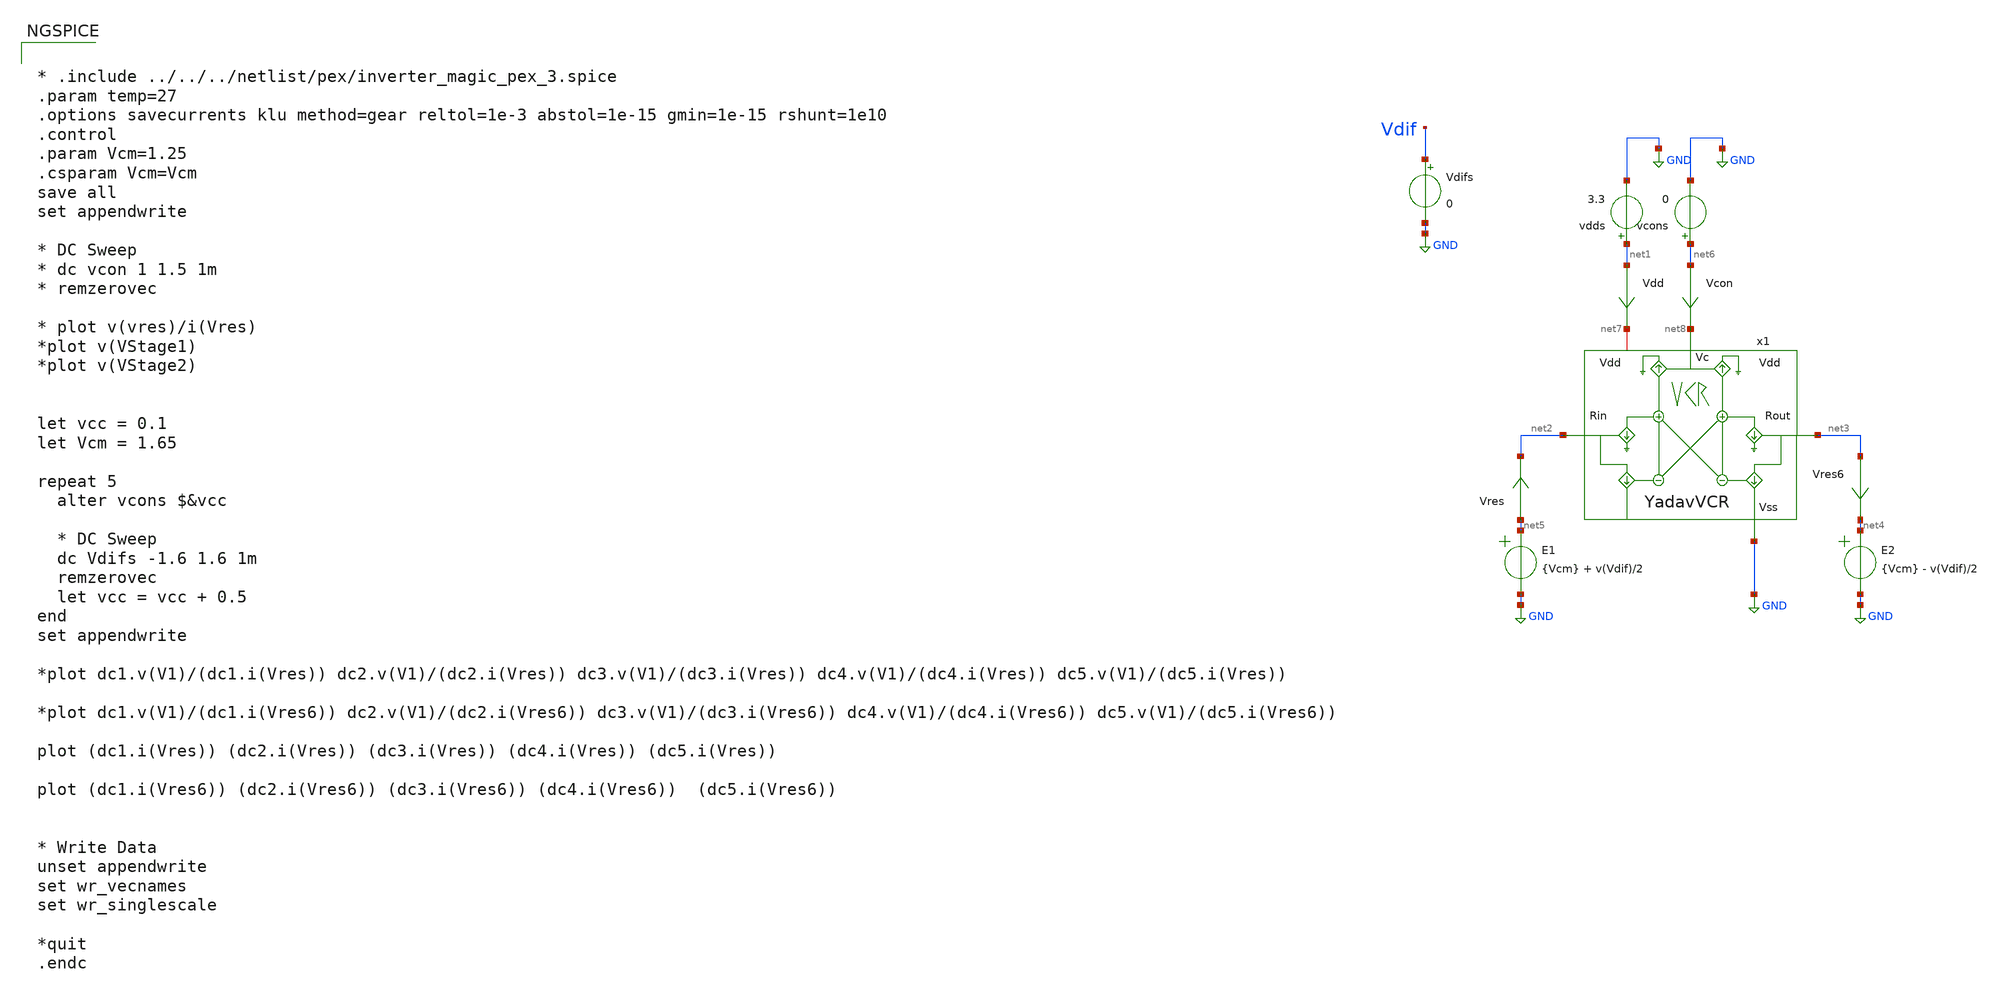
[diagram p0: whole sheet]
** sch_path: macros/heichips26_analog_project/macros/yadav/testbenches/xschem/plm.sch
**.subckt plm
Vres net5 net2 0
.save i(vres)
vdds net1 GND 3.3
Vdd net1 net7 0
.save i(vdd)
Vres6 net3 net4 0
.save i(vres6)
E1 net5 GND VOL=' {Vcm} + v(Vdif)/2 '
E2 net4 GND VOL=' {Vcm} - v(Vdif)/2 '
Vdifs Vdif GND 0
x1 net7 net2 net3 net8 GND YadavVCR
vcons net6 GND 0
Vcon net6 net8 0
.save i(vcon)
**** begin user architecture code


* .include ../../../netlist/pex/inverter_magic_pex_3.spice
.param temp=27
.options savecurrents klu method=gear reltol=1e-3 abstol=1e-15 gmin=1e-15 rshunt=1e10
.control
.param Vcm=1.25
.csparam Vcm=Vcm
save all
set appendwrite

* DC Sweep
* dc vcon 1 1.5 1m
* remzerovec

* plot v(vres)/i(Vres)
*plot v(VStage1)
*plot v(VStage2)


let vcc = 0.1
let Vcm = 1.65

repeat 5
  alter vcons $&vcc

  * DC Sweep
  dc Vdifs -1.6 1.6 1m
  remzerovec
  let vcc = vcc + 0.5
end
set appendwrite

*plot dc1.v(V1)/(dc1.i(Vres)) dc2.v(V1)/(dc2.i(Vres)) dc3.v(V1)/(dc3.i(Vres))
*+ dc4.v(V1)/(dc4.i(Vres)) dc5.v(V1)/(dc5.i(Vres))

*plot dc1.v(V1)/(dc1.i(Vres6)) dc2.v(V1)/(dc2.i(Vres6)) dc3.v(V1)/(dc3.i(Vres6))
*+ dc4.v(V1)/(dc4.i(Vres6)) dc5.v(V1)/(dc5.i(Vres6))

plot (dc1.i(Vres)) (dc2.i(Vres)) (dc3.i(Vres)) (dc4.i(Vres)) (dc5.i(Vres))

plot (dc1.i(Vres6)) (dc2.i(Vres6)) (dc3.i(Vres6)) (dc4.i(Vres6))  (dc5.i(Vres6))


* Write Data
unset appendwrite
set wr_vecnames
set wr_singlescale

*quit
.endc



.lib cornerMOSlv.lib mos_tt
.lib cornerMOShv.lib mos_tt
.lib cornerRES.lib res_typ
.lib cornerDIO.lib dio_tt

**** end user architecture code
**.ends

* expanding   symbol:  YadavVCR.sym # of pins=5
** sym_path: macros/heichips26_analog_project/macros/yadav/schematic/xschem/YadavVCR.sym
** sch_path: macros/heichips26_analog_project/macros/yadav/schematic/xschem/YadavVCR.sch
.subckt YadavVCR Vdd Rin Rout Vc Vss
*.ipin Vc
*.iopin Vss
*.iopin Vdd
*.ipin Rin
*.opin Rout
XM3 Vdd Rin net2 Vss sg13_hv_nmos w=0.72u l=4.14u ng=2 m=1 mm_ok=1
XM13 net1 net1 Vdd Vdd sg13_hv_pmos w=18.5u l=2.16u ng=2 m=1 mm_ok=1
XM1 net3 Rin Vss Vss sg13_hv_nmos w=0.72u l=4.14u ng=2 m=1 mm_ok=1
XM5 net1 net2 Vss Vss sg13_hv_nmos w=0.72u l=4.14u ng=2 m=1 mm_ok=1
XM2 net1 Rout Vss Vss sg13_hv_nmos w=0.72u l=4.14u ng=2 m=1 mm_ok=1
XM16 net3 net3 Vdd Vdd sg13_hv_pmos w=18.5u l=2.16u ng=2 m=1 mm_ok=1
XM7 net2 Vc Vss Vss sg13_hv_nmos w=0.72u l=4.14u ng=2 m=1 mm_ok=1
XM6 net3 net6 Vss Vss sg13_hv_nmos w=0.72u l=4.14u ng=2 m=1 mm_ok=1
XM14 net4 net1 Vdd Vdd sg13_hv_pmos w=18.5u l=2.16u ng=2 m=1 mm_ok=1
XM8 net6 Vc Vss Vss sg13_hv_nmos w=0.72u l=4.14u ng=2 m=1 mm_ok=1
XM4 Vdd Rout net6 Vss sg13_hv_nmos w=0.72u l=4.14u ng=2 m=1 mm_ok=1
XM9 net4 net4 Vss Vss sg13_hv_nmos w=0.72u l=2.16u ng=2 m=1 mm_ok=1
XM10 Rin net4 Vss Vss sg13_hv_nmos w=0.72u l=2.16u ng=2 m=1 mm_ok=1
XM17 Rin net3 Vdd Vdd sg13_hv_pmos w=18.5u l=2.16u ng=2 m=1 mm_ok=1
XM18 net5 net3 Vdd Vdd sg13_hv_pmos w=18.5u l=2.16u ng=2 m=1 mm_ok=1
XM11 net5 net5 Vss Vss sg13_hv_nmos w=0.72u l=2.16u ng=2 m=1 mm_ok=1
XM12 Rout net5 Vss Vss sg13_hv_nmos w=0.72u l=2.16u ng=2 m=1 mm_ok=1
XM15 Rout net1 Vdd Vdd sg13_hv_pmos w=18.5u l=2.16u ng=2 m=1 mm_ok=1
.ends

.GLOBAL GND
.end
